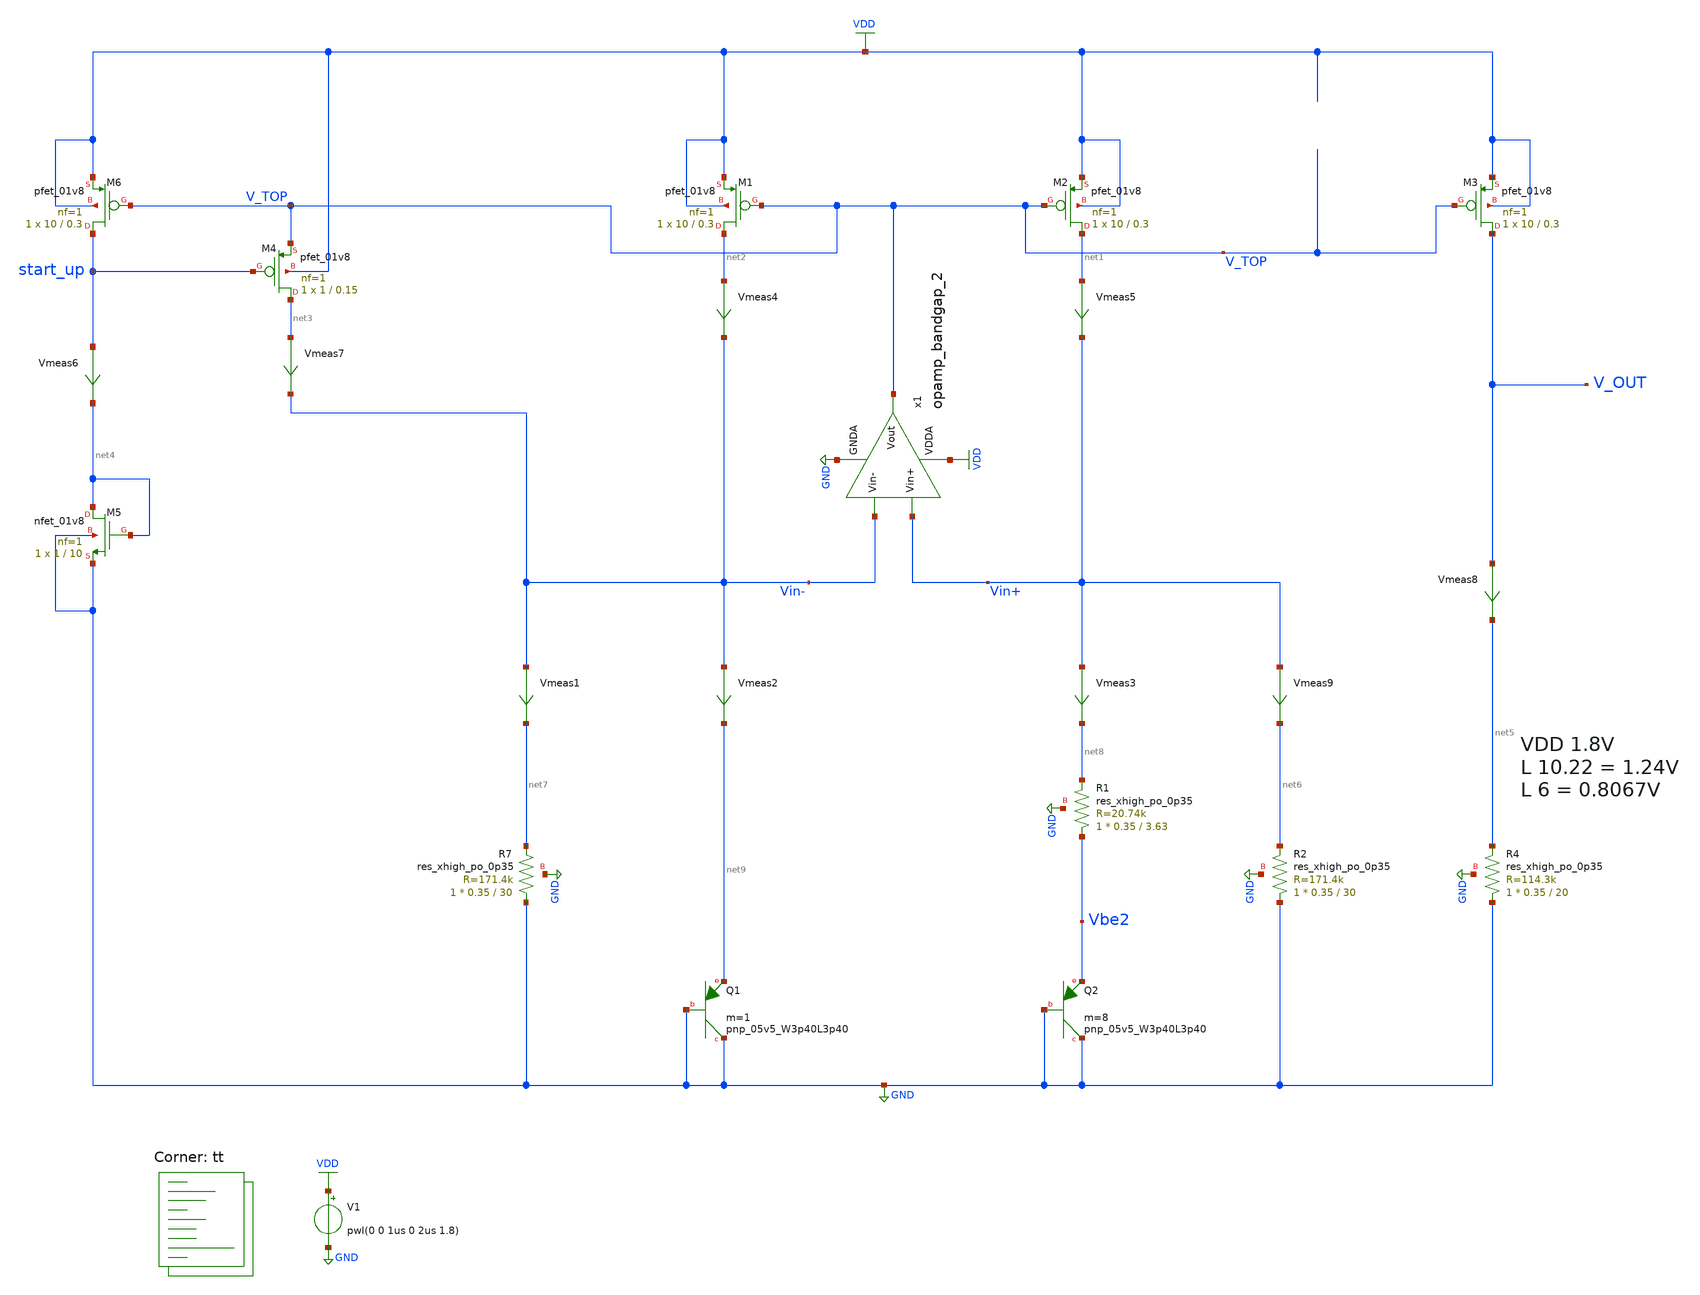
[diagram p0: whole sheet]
** sch_path: projects/bandgapref/xschem_ngspice/new_files/tb_low_voltage_BGR_10.sch
**.subckt tb_low_voltage_BGR_10
V1 VDD GND pwl(0 0 1us 0 2us 1.8)
XQ1 GND GND net9 sky130_fd_pr__pnp_05v5_W3p40L3p40 m=1
XQ2 GND GND Vbe2 sky130_fd_pr__pnp_05v5_W3p40L3p40 m=8
XM1 net2 V_TOP VDD VDD sky130_fd_pr__pfet_01v8 L=0.3 W=10 nf=1 ad='int((nf+1)/2) * W/nf * 0.29' as='int((nf+2)/2) * W/nf * 0.29'
+ pd='2*int((nf+1)/2) * (W/nf + 0.29)' ps='2*int((nf+2)/2) * (W/nf + 0.29)' nrd='0.29 / W' nrs='0.29 / W'
+ sa=0 sb=0 sd=0 mult=1 m=1
XM2 net1 V_TOP VDD VDD sky130_fd_pr__pfet_01v8 L=0.3 W=10 nf=1 ad='int((nf+1)/2) * W/nf * 0.29' as='int((nf+2)/2) * W/nf * 0.29'
+ pd='2*int((nf+1)/2) * (W/nf + 0.29)' ps='2*int((nf+2)/2) * (W/nf + 0.29)' nrd='0.29 / W' nrs='0.29 / W'
+ sa=0 sb=0 sd=0 mult=1 m=1
XM3 V_OUT V_TOP VDD VDD sky130_fd_pr__pfet_01v8 L=0.3 W=10 nf=1 ad='int((nf+1)/2) * W/nf * 0.29' as='int((nf+2)/2) * W/nf * 0.29'
+ pd='2*int((nf+1)/2) * (W/nf + 0.29)' ps='2*int((nf+2)/2) * (W/nf + 0.29)' nrd='0.29 / W' nrs='0.29 / W'
+ sa=0 sb=0 sd=0 mult=1 m=1
XR1 Vbe2 net8 GND sky130_fd_pr__res_xhigh_po_0p35 L=3.63 mult=1 m=1
XR2 GND net6 GND sky130_fd_pr__res_xhigh_po_0p35 L=30 mult=1 m=1
XR4 GND net5 GND sky130_fd_pr__res_xhigh_po_0p35 L=20 mult=1 m=1
Vmeas4 net2 Vin- 0
.save i(vmeas4)
XM5 net4 net4 GND GND sky130_fd_pr__nfet_01v8 L=10 W=1 nf=1 ad='int((nf+1)/2) * W/nf * 0.29' as='int((nf+2)/2) * W/nf * 0.29'
+ pd='2*int((nf+1)/2) * (W/nf + 0.29)' ps='2*int((nf+2)/2) * (W/nf + 0.29)' nrd='0.29 / W' nrs='0.29 / W'
+ sa=0 sb=0 sd=0 mult=1 m=1
XM6 start_up V_TOP VDD VDD sky130_fd_pr__pfet_01v8 L=0.3 W=10 nf=1 ad='int((nf+1)/2) * W/nf * 0.29' as='int((nf+2)/2) * W/nf * 0.29'
+ pd='2*int((nf+1)/2) * (W/nf + 0.29)' ps='2*int((nf+2)/2) * (W/nf + 0.29)' nrd='0.29 / W' nrs='0.29 / W'
+ sa=0 sb=0 sd=0 mult=1 m=1
Vmeas5 net1 Vin+ 0
.save i(vmeas5)
XM4 net3 start_up V_TOP VDD sky130_fd_pr__pfet_01v8 L=0.15 W=1 nf=1 ad='int((nf+1)/2) * W/nf * 0.29'
+ as='int((nf+2)/2) * W/nf * 0.29' pd='2*int((nf+1)/2) * (W/nf + 0.29)' ps='2*int((nf+2)/2) * (W/nf + 0.29)'
+ nrd='0.29 / W' nrs='0.29 / W' sa=0 sb=0 sd=0 mult=1 m=1
Vmeas7 net3 Vin- 0
.save i(vmeas7)
XR7 GND net7 GND sky130_fd_pr__res_xhigh_po_0p35 L=30 mult=1 m=1
Vmeas8 V_OUT net5 0
.save i(vmeas8)
Vmeas6 start_up net4 0
.save i(vmeas6)
Vmeas1 Vin- net7 0
.save i(vmeas1)
Vmeas2 Vin- net9 0
.save i(vmeas2)
Vmeas3 Vin+ net8 0
.save i(vmeas3)
Vmeas9 Vin+ net6 0
.save i(vmeas9)
x1 VDD V_TOP Vin- Vin+ GND opamp_bandgap_2
**** begin user architecture code
.lib $::SKYWATER_MODELS/sky130.lib.spice tt



* ngspice commands


.option method=gear
.option wnflag=1
.option savecurrents
* .temp =140

.save @m.xm1.msky130_fd_pr__pfet_01v8[gm] @m.xm1.msky130_fd_pr__pfet_01v8[vth] @m.xm1.msky130_fd_pr__pfet_01v8[vgs] @m.xm1.msky130_fd_pr__pfet_01v8[vds] @m.xm2.msky130_fd_pr__pfet_01v8[gm] @m.xm2.msky130_fd_pr__pfet_01v8[vth] @m.xm2.msky130_fd_pr__pfet_01v8[vgs] @m.xm2.msky130_fd_pr__pfet_01v8[vds] @m.xm3.msky130_fd_pr__pfet_01v8[gm] @m.xm4.msky130_fd_pr__pfet_01v8[gm] @m.xm4.msky130_fd_pr__pfet_01v8[vth] @m.xm5.msky130_fd_pr__nfet_01v8[gm] @m.xm5.msky130_fd_pr__nfet_01v8[vth] @m.xm6.msky130_fd_pr__pfet_01v8[gm] @m.xm6.msky130_fd_pr__pfet_01v8[vth] @m.xm7.msky130_fd_pr__nfet_01v8[gm] @m.xm7.msky130_fd_pr__nfet_01v8[vth] @m.xm8.msky130_fd_pr__nfet_01v8[gm] @m.xm8.msky130_fd_pr__nfet_01v8[vth] @m.xm9.msky130_fd_pr__nfet_01v8[gm] @m.xm9.msky130_fd_pr__nfet_01v8[vth] @m.x1.xm1.msky130_fd_pr__nfet_01v8[gm] @m.x1.xm2.msky130_fd_pr__nfet_01v8[gm] @m.x1.xm3.msky130_fd_pr__nfet_01v8[gm] @m.x1.xm4.msky130_fd_pr__nfet_01v8[gm] @m.x1.xm5.msky130_fd_pr__pfet_01v8[gm] @m.x1.xm6.msky130_fd_pr__nfet_01v8[gm] @m.x1.xm7.msky130_fd_pr__pfet_01v8[gm]

* .ic v(vin-) = 0.8
* .ic v(vin+) = 0.8
* .ic v(v_top) = 1.8

.control

    save all
    * dc temp -40 120 5 V1 1.6 2.0 0.05
    * dc V1 1.7 1.9 0.001 temp -40 120 40
    * dc V1 0.0 2.0 0.02 temp -40 120 40
    * dc V1 0 2.0 0.02
    tran 1ns 8us
    remzerovec
    write tb_low_voltage_BGR_10.raw
    * write tb_low_voltage_BGR_10_2.raw
    * write tb_low_voltage_BGR_10_3.raw
.endc







.option method=gear
.option wnflag=1
.option savecurrents
* .temp =140

.save @m.xm1.msky130_fd_pr__pfet_01v8[gm] @m.xm1.msky130_fd_pr__pfet_01v8[vth] @m.xm1.msky130_fd_pr__pfet_01v8[vgs] @m.xm1.msky130_fd_pr__pfet_01v8[vds] @m.xm2.msky130_fd_pr__pfet_01v8[gm] @m.xm2.msky130_fd_pr__pfet_01v8[vth] @m.xm2.msky130_fd_pr__pfet_01v8[vgs] @m.xm2.msky130_fd_pr__pfet_01v8[vds] @m.xm3.msky130_fd_pr__pfet_01v8[gm] @m.xm4.msky130_fd_pr__pfet_01v8[gm] @m.xm4.msky130_fd_pr__nfet_01v8[gm] @m.x1.xm1.msky130_fd_pr__nfet_01v8[gm] @m.x1.xm2.msky130_fd_pr__nfet_01v8[gm] @m.x1.xm3.msky130_fd_pr__nfet_01v8[gm] @m.x1.xm4.msky130_fd_pr__pfet_01v8[gm] @m.x1.xm5.msky130_fd_pr__pfet_01v8[gm] @m.x1.xm6.msky130_fd_pr__nfet_01v8[gm] @m.x1.xm7.msky130_fd_pr__pfet_01v8[gm] @m.x2.xm1.msky130_fd_pr__nfet_01v8[gm] @m.x2.xm2.msky130_fd_pr__nfet_01v8[gm] @m.x2.xm3.msky130_fd_pr__nfet_01v8[gm] @m.x2.xm4.msky130_fd_pr__pfet_01v8[gm] @m.x2.xm5.msky130_fd_pr__pfet_01v8[gm] @m.x2.xm6.msky130_fd_pr__pfet_01v8[gm] @m.x2.xm7.msky130_fd_pr__pfet_01v8[gm]

* .ic v(vin-) = 0.8
* .ic v(vin+) = 0.8
* .ic v(v_top) = 1.8

.control

  * let start_vdd = 0.3
  * let stop_vdd = 1.8
  * let delta_vdd = 0.3
  * let w_act = start_vdd
  * while w_act le stop_vdd
    * echo $&w_act
    * alter V1 = w_act
    * echo v[vdd]
    * alter @V1[pwl] = [ 0 0 1us 0 2us $&w_act ]
    * reset
    save all
    * run
    * dc temp -40 120 5 V1 1.6 2.0 0.05
    * dc V1 1.7 1.9 0.001 temp -40 120 40
    * dc V1 0.0 2.0 0.01 temp -40 120 40
    * dc V1 0 2.0 0.001
    tran 1ns 8us
    remzerovec
    * write tb_low_voltage_BGR_6.raw
    * write tb_low_voltage_BGR_6_2.raw
    * write tb_low_voltage_BGR_6_3.raw
    write tb_low_voltage_BGR_6_4.raw
    * let w_act = w_act + delta_vdd
    set appendwrite
  * end

.endc



**** end user architecture code
**.ends

* expanding   symbol:
*+  /foss/designs/my_design/projects/bandgapref/xschem_ngspice/new_files/opamp_bandgap_2.sym # of pins=5
** sym_path: projects/bandgapref/xschem_ngspice/new_files/opamp_bandgap_2.sym
** sch_path: projects/bandgapref/xschem_ngspice/new_files/opamp_bandgap_2.sch
.subckt opamp_bandgap_2 VDDA Vout Vin- Vin+ GNDA
*.ipin Vin+
*.opin Vout
*.ipin Vin-
*.ipin GNDA
*.ipin VDDA
XM1 V_p VDDA GNDA GNDA sky130_fd_pr__nfet_01v8 L=10 W=5 nf=1 ad='int((nf+1)/2) * W/nf * 0.29' as='int((nf+2)/2) * W/nf * 0.29'
+ pd='2*int((nf+1)/2) * (W/nf + 0.29)' ps='2*int((nf+2)/2) * (W/nf + 0.29)' nrd='0.29 / W' nrs='0.29 / W'
+ sa=0 sb=0 sd=0 mult=1 m=1
XM2 V_mirror Vin- V_p GNDA sky130_fd_pr__nfet_01v8 L=0.2 W=5 nf=1 ad='int((nf+1)/2) * W/nf * 0.29' as='int((nf+2)/2) * W/nf * 0.29'
+ pd='2*int((nf+1)/2) * (W/nf + 0.29)' ps='2*int((nf+2)/2) * (W/nf + 0.29)' nrd='0.29 / W' nrs='0.29 / W'
+ sa=0 sb=0 sd=0 mult=1 m=1
XM3 1st_Vout Vin+ V_p GNDA sky130_fd_pr__nfet_01v8 L=0.2 W=5 nf=1 ad='int((nf+1)/2) * W/nf * 0.29' as='int((nf+2)/2) * W/nf * 0.29'
+ pd='2*int((nf+1)/2) * (W/nf + 0.29)' ps='2*int((nf+2)/2) * (W/nf + 0.29)' nrd='0.29 / W' nrs='0.29 / W'
+ sa=0 sb=0 sd=0 mult=1 m=1
XM5 V_mirror V_mirror VDDA VDDA sky130_fd_pr__pfet_01v8 L=0.2 W=10 nf=2 ad='int((nf+1)/2) * W/nf * 0.29'
+ as='int((nf+2)/2) * W/nf * 0.29' pd='2*int((nf+1)/2) * (W/nf + 0.29)' ps='2*int((nf+2)/2) * (W/nf + 0.29)'
+ nrd='0.29 / W' nrs='0.29 / W' sa=0 sb=0 sd=0 mult=1 m=1
XM6 1st_Vout V_mirror VDDA VDDA sky130_fd_pr__pfet_01v8 L=0.2 W=10 nf=2 ad='int((nf+1)/2) * W/nf * 0.29'
+ as='int((nf+2)/2) * W/nf * 0.29' pd='2*int((nf+1)/2) * (W/nf + 0.29)' ps='2*int((nf+2)/2) * (W/nf + 0.29)'
+ nrd='0.29 / W' nrs='0.29 / W' sa=0 sb=0 sd=0 mult=1 m=1
XM4 Vout VDDA GNDA GNDA sky130_fd_pr__nfet_01v8 L=10 W=5 nf=1 ad='int((nf+1)/2) * W/nf * 0.29' as='int((nf+2)/2) * W/nf * 0.29'
+ pd='2*int((nf+1)/2) * (W/nf + 0.29)' ps='2*int((nf+2)/2) * (W/nf + 0.29)' nrd='0.29 / W' nrs='0.29 / W'
+ sa=0 sb=0 sd=0 mult=1 m=1
XM7 Vout 1st_Vout VDDA VDDA sky130_fd_pr__pfet_01v8 L=0.2 W=10 nf=2 ad='int((nf+1)/2) * W/nf * 0.29'
+ as='int((nf+2)/2) * W/nf * 0.29' pd='2*int((nf+1)/2) * (W/nf + 0.29)' ps='2*int((nf+2)/2) * (W/nf + 0.29)'
+ nrd='0.29 / W' nrs='0.29 / W' sa=0 sb=0 sd=0 mult=1 m=1
.ends

.GLOBAL GND
.GLOBAL VDD
.end
